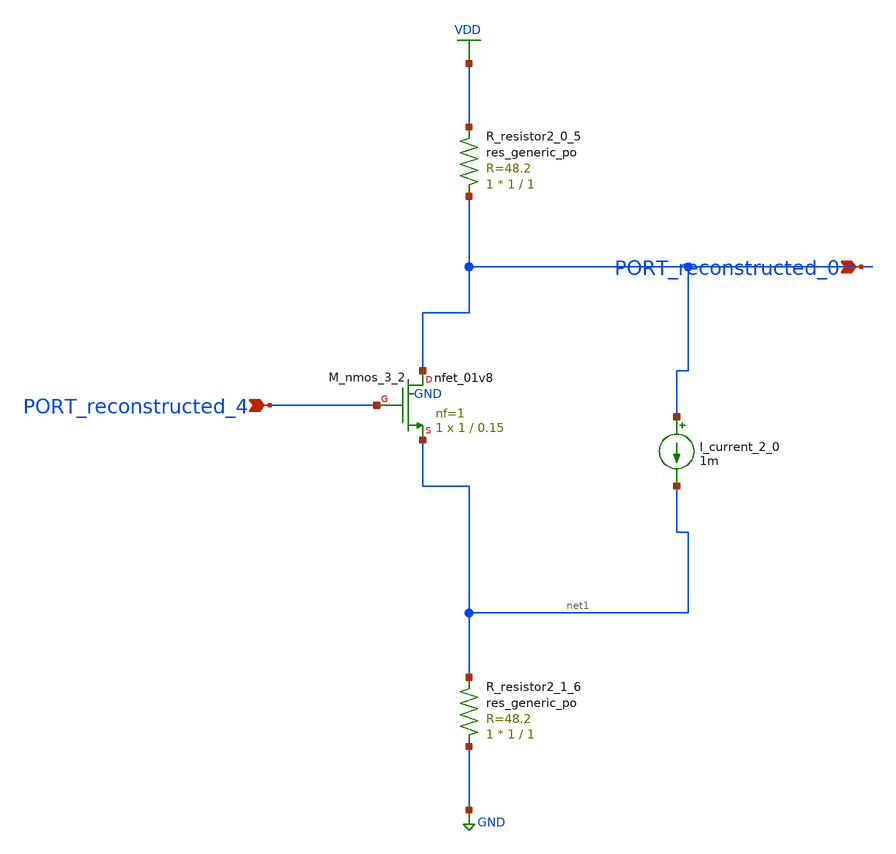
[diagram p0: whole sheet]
** sch_path: schematics/AMSNet/450.sch
**.subckt 450 PORT_reconstructed_4 PORT_reconstructed_0
*.ipin PORT_reconstructed_4
*.ipin PORT_reconstructed_0
I_current_2_0 PORT_reconstructed_0 net1 1m
XM_nmos_3_2 PORT_reconstructed_0 PORT_reconstructed_4 net1 GND sky130_fd_pr__nfet_01v8 L=0.15 W=1 nf=1
+ ad='int((1 + 1)/2) * 1 / 1 * 0.29' as='int((1 + 2)/2) * 1 / 1 * 0.29' pd='2*int((1 + 1)/2) * (1 / 1 + 0.29)'
+ ps='2*int((1 + 2)/2) * (1 / 1 + 0.29)' nrd='0.29 / 1 ' nrs='0.29 / 1 ' sa=0 sb=0 sd=0 mult=1 m=1
XR_resistor2_0_5 PORT_reconstructed_0 VDD sky130_fd_pr__res_generic_po W=1 L=1 m=1
XR_resistor2_1_6 GND net1 sky130_fd_pr__res_generic_po W=1 L=1 m=1
**.ends
.GLOBAL GND
.GLOBAL VDD
.end
